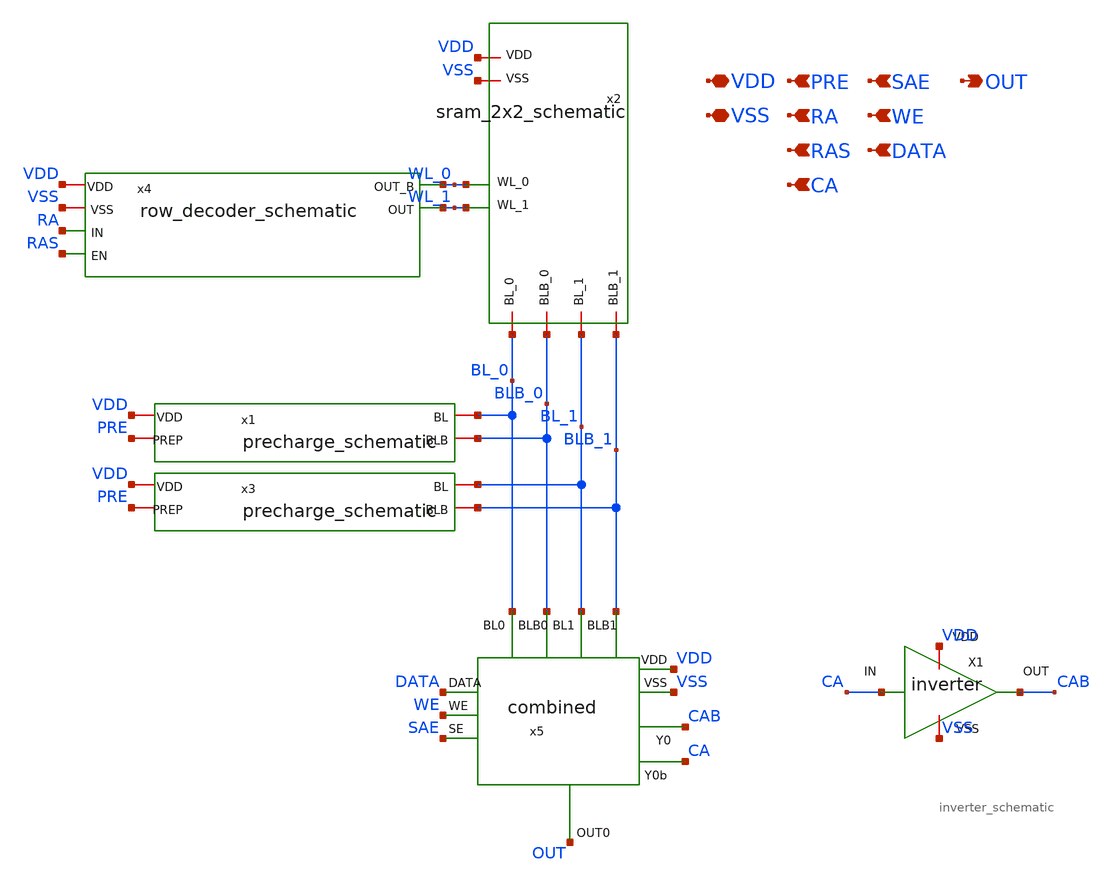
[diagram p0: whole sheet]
** sch_path: SRAM/top_module/schematic/sram_top_module_schematic.sch
**.subckt sram_top_module_schematic VDD VSS RA RAS PRE SAE DATA WE CA OUT
*.iopin VDD
*.iopin VSS
*.ipin RA
*.ipin RAS
*.ipin PRE
*.ipin SAE
*.ipin DATA
*.ipin WE
*.ipin CA
*.opin OUT
x2 BL_0 BLB_1 BLB_0 BL_1 VDD VSS WL_0 WL_1 sram_2x2_schematic
x1 VDD PRE BL_0 BLB_0 precharge_schematic
x3 VDD PRE BL_1 BLB_1 precharge_schematic
x4 VDD RA WL_1 VSS WL_0 RAS row_decoder_schematic
x5 BLB_1 BLB_0 BL_0 BL_1 DATA WE SAE VDD VSS CAB CA OUT combined
x6 VDD CA CAB VSS inverter_schematic
**.ends

* expanding   symbol:  sram_2x2_schematic.sym # of pins=8
** sym_path: SRAM/2x2/schematic/sram_2x2_schematic.sym
** sch_path: SRAM/2x2/schematic/sram_2x2_schematic.sch
.subckt sram_2x2_schematic BL_0 BLB_1 BLB_0 BL_1 VDD VSS WL_0 WL_1
*.ipin WL_0
*.ipin WL_1
*.iopin BL_0
*.iopin BLB_0
*.iopin BL_1
*.iopin BLB_1
*.iopin VDD
*.iopin VSS
X1 WL_0 BL_0 BLB_0 VDD VSS sram_cell_schematic
X2 WL_0 BL_1 BLB_1 VDD VSS sram_cell_schematic
X3 WL_1 BL_0 BLB_0 VDD VSS sram_cell_schematic
X4 WL_1 BL_1 BLB_1 VDD VSS sram_cell_schematic
.ends


* expanding   symbol:  precharge_schematic.sym # of pins=4
** sym_path: SRAM/precharge/schematic/precharge_schematic.sym
** sch_path: SRAM/precharge/schematic/precharge_schematic.sch
.subckt precharge_schematic VDD PREP BL BLB
*.iopin VDD
*.iopin BL
*.iopin BLB
*.iopin PREP
M3 VDD PREP BL VDD pfet w=7.2u l=0.6u m=1
M1 BLB PREP VDD VDD pfet w=7.2u l=0.6u m=1
M2 BL PREP BLB VDD pfet w=7.2u l=0.6u m=1
.ends


* expanding   symbol:  row_decoder_schematic.sym # of pins=6
** sym_path: SRAM/row_decoder/schematic/row_decoder_schematic.sym
** sch_path: SRAM/row_decoder/schematic/row_decoder_schematic.sch
.subckt row_decoder_schematic VDD IN OUT VSS OUT_B EN
*.iopin VDD
*.iopin VSS
*.ipin IN
*.ipin EN
*.opin OUT
*.opin OUT_B
x1 VDD net2 EN net3 VSS nand_schematic
x2 VDD net1 EN net4 VSS nand_schematic
x3 VDD net1 net2 VSS inverter_schematic
x4 VDD IN net1 VSS inverter_schematic
x5 VDD net3 OUT VSS inverter_schematic
x6 VDD net4 OUT_B VSS inverter_schematic
.ends


* expanding   symbol:  combined.sym # of pins=12
** sym_path: SRAM/combined_mux_sa_wrd/schematic/combined.sym
** sch_path: SRAM/combined_mux_sa_wrd/schematic/combined.sch
.subckt combined BLB1 BLB0 BL0 BL1 DATA WE SE VDD VSS Y0 Y0b OUT0
*.ipin BL0
*.ipin BLB0
*.ipin BL1
*.ipin BLB1
*.ipin DATA
*.ipin WE
*.ipin SE
*.iopin VDD
*.iopin VSS
*.ipin Y0
*.opin OUT0
*.ipin Y0b
x5 MUX_OUT MUX_OUTB WE VDD DATA VSS WR_Drive
x1 BL0 BLB0 BL1 BLB1 VDD VSS Y0 Y0b MUX_OUT MUX_OUTB MUX1
x2 VDD OUT0 MUX_OUTB MUX_OUT SE VSS Senseamp
.ends


* expanding   symbol:  inverter_schematic.sym # of pins=4
** sym_path: SRAM/inverter/schematic/inverter_schematic.sym
** sch_path: SRAM/inverter/schematic/inverter_schematic.sch
.subckt inverter_schematic VDD IN OUT VSS
*.ipin IN
*.opin OUT
*.iopin VSS
*.iopin VDD
M2 OUT IN VSS VSS nfet w=1.8u l=0.6u m=1
M1 OUT IN VDD VDD pfet w=4.2u l=0.6u m=1
.ends


* expanding   symbol:  sram_cell_schematic.sym # of pins=5
** sym_path: SRAM/cell/schematic/sram_cell_schematic.sym
** sch_path: SRAM/cell/schematic/sram_cell_schematic.sch
.subckt sram_cell_schematic WL BL BLB VDD VSS
*.ipin WL
*.iopin BL
*.iopin BLB
*.iopin VDD
*.iopin VSS
M4 VSS Q QB VSS nfet w=3.6u l=0.6u m=1
M5 QB Q VDD VDD pfet w=3.6u l=0.6u m=1
M6 Q QB VDD VDD pfet w=3.6u l=0.6u m=1
M1 Q WL BL VSS nfet w=1.8u l=0.6u m=1
M3 VSS QB Q VSS nfet w=3.6u l=0.6u m=1
M2 BLB WL QB VSS nfet w=1.8u l=0.6u m=1
.ends


* expanding   symbol:  nand_schematic.sym # of pins=5
** sym_path: SRAM/nand/schematic/nand_schematic.sym
** sch_path: SRAM/nand/schematic/nand_schematic.sch
.subckt nand_schematic VDD A B OUT VSS
*.iopin VDD
*.iopin VSS
*.iopin A
*.iopin B
*.iopin OUT
M1 OUT A VDD VDD pfet w=4.2u l=0.6u m=1
M2 OUT B VDD VDD pfet w=4.2u l=0.6u m=1
M3 OUT B net1 VSS nfet w=3.6u l=0.6u m=1
M4 net1 A VSS VSS nfet w=3.6u l=0.6u m=1
.ends


* expanding   symbol:  WR_Drive.sym # of pins=6
** sym_path: SRAM/wr_driver/schematic/WR_Drive.sym
** sch_path: SRAM/wr_driver/schematic/WR_Drive.sch
.subckt WR_Drive BL BLB WE VDD DATA VSS
*.ipin WE
*.ipin DATA
*.iopin VDD
*.iopin VSS
*.opin BL
*.opin BLB
M1 net1 WE VSS VSS nfet w=3.6u l=0.6u m=1
M4 net2 DATA VDD VDD pfet w=36u l=0.6u m=1
M5 net3 net2 VSS VSS nfet w=18u l=0.6u m=1
M6 net3 net2 VDD VDD pfet w=36u l=0.6u m=1
M7 net2 net1 BLB VDD pfet w=14.4u l=0.6u m=1
M8 BLB WE net2 VSS nfet w=7.2u l=0.6u m=1
M2 net1 WE VDD VDD pfet w=7.2u l=0.6u m=1
M3 net2 DATA VSS VSS nfet w=18u l=0.6u m=1
M9 BL WE net3 VSS nfet w=7.2u l=0.6u m=1
M10 net3 net1 BL VDD pfet w=14.4u l=0.6u m=1
.ends


* expanding   symbol:  MUX1.sym # of pins=10
** sym_path: SRAM/mux/schematic/MUX1.sym
** sch_path: SRAM/mux/schematic/MUX1.sch
.subckt MUX1 BL0 BLB0 BL1 BLB1 VDD VSS Y0 Y0b MUX_OUT MUX_OUTB
*.iopin BL0
*.iopin BLB0
*.iopin BL1
*.iopin BLB1
*.iopin VDD
*.iopin VSS
*.iopin Y0
*.iopin Y0b
*.opin MUX_OUT
*.opin MUX_OUTB
M1 BL0 Y0b MUX_OUT VDD pfet w=4.2u l=0.6u m=1
M2 BLB0 Y0b MUX_OUTB VDD pfet w=4.2u l=0.6u m=1
M3 BL1 Y0 MUX_OUT VDD pfet w=4.2u l=0.6u m=1
M4 BLB1 Y0 MUX_OUTB VDD pfet w=4.2u l=0.6u m=1
M5 BL0 Y0 MUX_OUT VSS nfet w=1.8u l=0.6u m=1
M6 BLB0 Y0 MUX_OUTB VSS nfet w=1.8u l=0.6u m=1
M7 BL1 Y0b MUX_OUT VSS nfet w=1.8u l=0.6u m=1
M8 BLB1 Y0b MUX_OUTB VSS nfet w=1.8u l=0.6u m=1
.ends


* expanding   symbol:  Senseamp.sym # of pins=6
** sym_path: SRAM/senseamp/schematic/Senseamp.sym
** sch_path: SRAM/senseamp/schematic/Senseamp.sch
.subckt Senseamp VDD OUT0 BLB BL SE VSS
*.ipin BLB
*.ipin BL
*.ipin SE
*.opin OUT0
*.iopin VSS
*.iopin VDD
M7 net2 net1 VDD VDD pfet w=3.6u l=0.6u m=1
M9 OUT0 net2 VDD VDD pfet w=3.6u l=0.6u m=1
M1 net1 BLB net3 VSS nfet w=1.2u l=0.6u m=1
M2 net3 SE VSS VSS nfet w=3.6u l=0.6u m=1
M3 net2 BL net3 VSS nfet w=1.2u l=0.6u m=1
M4 OUT0 SE VSS VSS nfet w=1.8u l=0.6u m=1
M5 net1 net1 VDD VDD pfet w=3.6u l=0.6u m=1
.ends

.end
